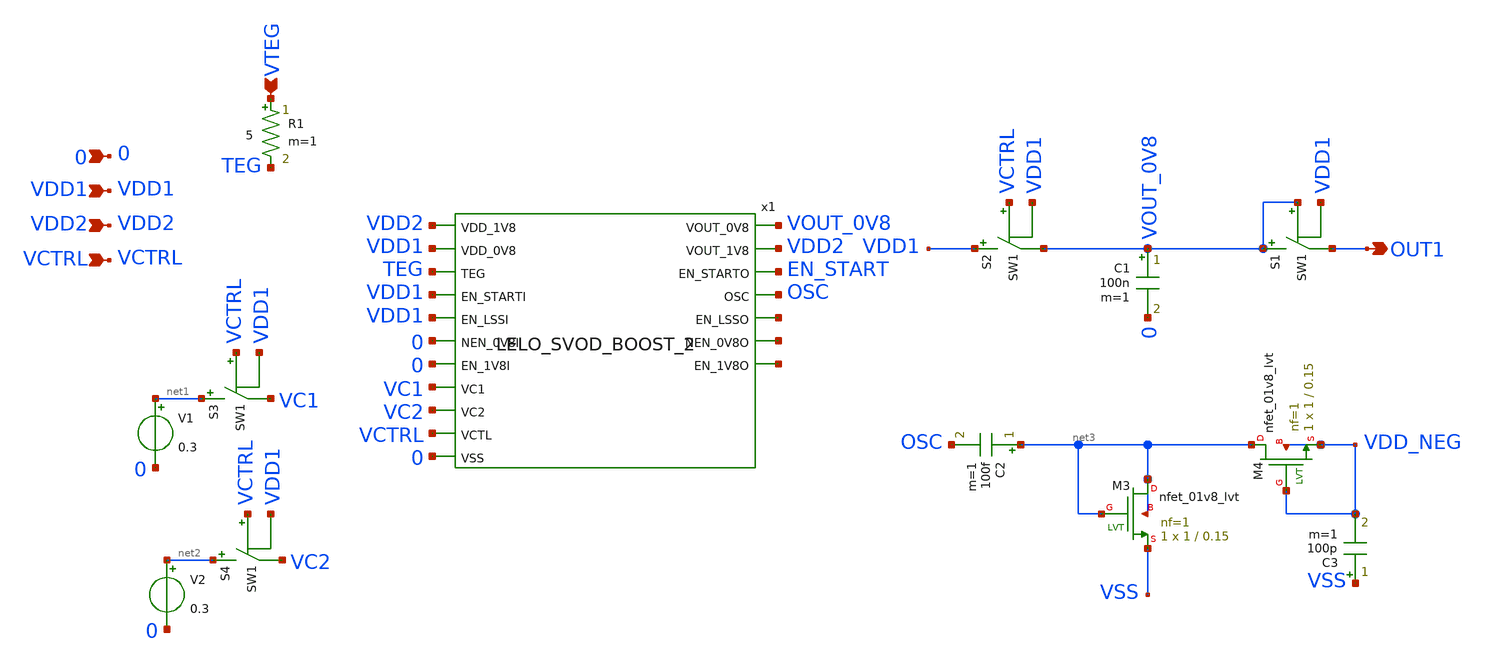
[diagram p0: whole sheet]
** sch_path: design/LELO_SVOD_SKY130A/LELO_SVOD_0V8_BOOST.sch
**.subckt LELO_SVOD_0V8_BOOST OUT1 VTEG 0 VDD1 VDD2 VCTRL
*.opin OUT1
*.ipin VTEG
*.ipin 0
*.ipin VDD1
*.ipin VDD2
*.ipin VCTRL
S1 VOUT_0V8 OUT1 VOUT_0V8 VDD1 SW1
x1 VOUT_0V8 VDD2 VDD1 TEG VDD1 VDD1 0 0 VDD2 VC1 VC2 VCTRL 0 EN_START OSC net4 net5 net6
+ LELO_SVOD_BOOST_2
C1 VOUT_0V8 0 100n m=1
R1 VTEG TEG 5 m=1
V1 net1 0 0.3
V2 net2 0 0.3
S2 VDD1 VOUT_0V8 VCTRL VDD1 SW1
S3 net1 VC1 VCTRL VDD1 SW1
S4 net2 VC2 VCTRL VDD1 SW1
C2 net3 OSC 100f m=1
XM3 net3 net3 VSS net3 sky130_fd_pr__nfet_01v8_lvt L=0.15 W=1 nf=1 ad='int((1 + 1)/2) * 1 / 1 * 0.29'
+ as='int((1 + 2)/2) * 1 / 1 * 0.29' pd='2*int((1 + 1)/2) * (1 / 1 + 0.29)' ps='2*int((1 + 2)/2) * (1 / 1 + 0.29)'
+ nrd='0.29 / 1 ' nrs='0.29 / 1 ' sa=0 sb=0 sd=0 mult=1 m=1
XM4 net3 VDD_NEG VDD_NEG VDD_NEG sky130_fd_pr__nfet_01v8_lvt L=0.15 W=1 nf=1 ad='int((1 + 1)/2) * 1 / 1 * 0.29'
+ as='int((1 + 2)/2) * 1 / 1 * 0.29' pd='2*int((1 + 1)/2) * (1 / 1 + 0.29)' ps='2*int((1 + 2)/2) * (1 / 1 + 0.29)'
+ nrd='0.29 / 1 ' nrs='0.29 / 1 ' sa=0 sb=0 sd=0 mult=1 m=1
C3 VSS VDD_NEG 100p m=1
**.ends
**** begin user architecture code
.MODEL SW1 SW   VT=0 VH=0.001  RON=0.001 ROFF=10G
**** end user architecture code
.end
